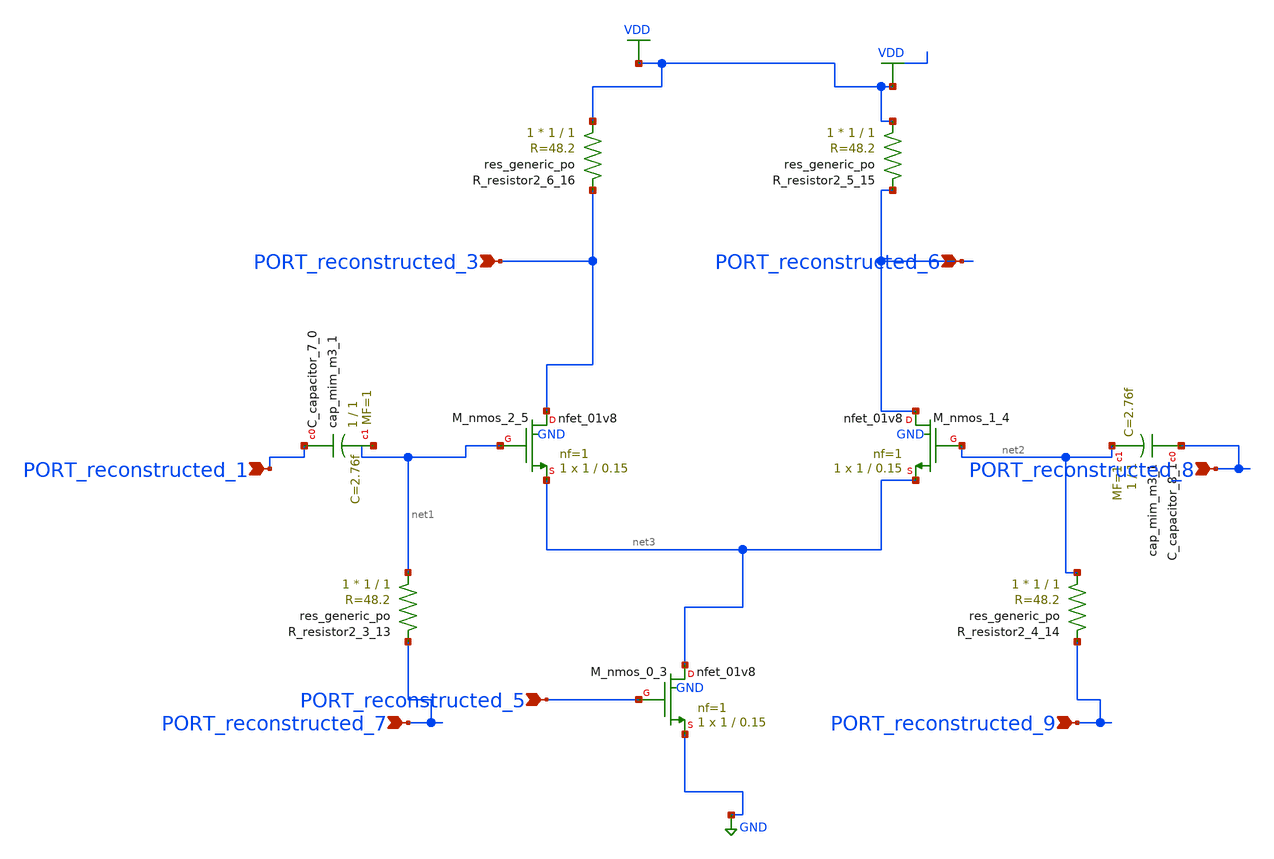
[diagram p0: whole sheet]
** sch_path: schematics/SchemGen/10_1109_ACCESS_2021_3064007_05_001.sch
**.subckt 10_1109_ACCESS_2021_3064007_05_001 PORT_reconstructed_5 PORT_reconstructed_3
*+ PORT_reconstructed_6 PORT_reconstructed_1 PORT_reconstructed_7 PORT_reconstructed_8 PORT_reconstructed_9
*.ipin PORT_reconstructed_5
*.ipin PORT_reconstructed_3
*.ipin PORT_reconstructed_6
*.ipin PORT_reconstructed_1
*.ipin PORT_reconstructed_7
*.ipin PORT_reconstructed_8
*.ipin PORT_reconstructed_9
XC_capacitor_7_0 PORT_reconstructed_1 net1 sky130_fd_pr__cap_mim_m3_1 W=1 L=1 MF=1 m=1
XC_capacitor_8_1 PORT_reconstructed_8 net2 sky130_fd_pr__cap_mim_m3_1 W=1 L=1 MF=1 m=1
XM_nmos_0_3 net3 PORT_reconstructed_5 GND GND sky130_fd_pr__nfet_01v8 L=0.15 W=1 nf=1 ad='int((1 + 1)/2) * 1 / 1 * 0.29'
+ as='int((1 + 2)/2) * 1 / 1 * 0.29' pd='2*int((1 + 1)/2) * (1 / 1 + 0.29)' ps='2*int((1 + 2)/2) * (1 / 1 + 0.29)'
+ nrd='0.29 / 1 ' nrs='0.29 / 1 ' sa=0 sb=0 sd=0 mult=1 m=1
XM_nmos_1_4 PORT_reconstructed_6 net2 net3 GND sky130_fd_pr__nfet_01v8 L=0.15 W=1 nf=1 ad='int((1 + 1)/2) * 1 / 1 * 0.29'
+ as='int((1 + 2)/2) * 1 / 1 * 0.29' pd='2*int((1 + 1)/2) * (1 / 1 + 0.29)' ps='2*int((1 + 2)/2) * (1 / 1 + 0.29)'
+ nrd='0.29 / 1 ' nrs='0.29 / 1 ' sa=0 sb=0 sd=0 mult=1 m=1
XM_nmos_2_5 PORT_reconstructed_3 net1 net3 GND sky130_fd_pr__nfet_01v8 L=0.15 W=1 nf=1 ad='int((1 + 1)/2) * 1 / 1 * 0.29'
+ as='int((1 + 2)/2) * 1 / 1 * 0.29' pd='2*int((1 + 1)/2) * (1 / 1 + 0.29)' ps='2*int((1 + 2)/2) * (1 / 1 + 0.29)'
+ nrd='0.29 / 1 ' nrs='0.29 / 1 ' sa=0 sb=0 sd=0 mult=1 m=1
XR_resistor2_3_13 net1 PORT_reconstructed_7 sky130_fd_pr__res_generic_po W=1 L=1 m=1
XR_resistor2_4_14 net2 PORT_reconstructed_9 sky130_fd_pr__res_generic_po W=1 L=1 m=1
XR_resistor2_5_15 VDD PORT_reconstructed_6 sky130_fd_pr__res_generic_po W=1 L=1 m=1
XR_resistor2_6_16 VDD PORT_reconstructed_3 sky130_fd_pr__res_generic_po W=1 L=1 m=1
**.ends
.GLOBAL GND
.GLOBAL VDD
.end
